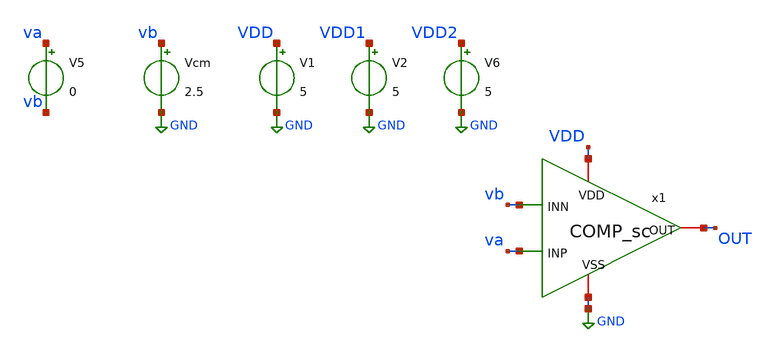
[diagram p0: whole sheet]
** sch_path: FINAL/XSCHEM/TEST_TOTAL/test_TOTAL.sch
**.subckt test_TOTAL
V1 VDD GND 5
V2 VDD1 GND 5
V6 VDD2 GND 5
V5 va vb 0
Vcm vb GND 2.5
x1 VDD vb OUT va GND COMP_sc
**** begin user architecture code

.include $::180MCU_MODELS/design.ngspice
.lib $::180MCU_MODELS/sm141064.ngspice typical
.lib $::180MCU_MODELS/sm141064.ngspice cap_mim
.lib $::180MCU_MODELS/sm141064.ngspice res_typical
.lib $::180MCU_MODELS/sm141064.ngspice moscap_typical
.lib $::180MCU_MODELS/sm141064.ngspice mimcap_typical


.include ../../../../Layouts/COMP/mag/COMP_pex_rc.spice
Xextrc GND VDD1 OUT1 va vb COMP
*COMP VSS VDD OUT INP INN


* The v2 layout, beside v1. The subcircuit is renamed to COMP_V2 because both
* extractions declare the same name -- the cell is named the same on purpose,
* which is what allows comparing them against the SAME reference in
* LVS. preparar_extraidos.sh renames it, touching only .subckt and .ends.
.include ../../../../layouts_v2/COMP/mag/COMP_V2_pex_rc.spice
Xextrc2 GND VDD2 OUT2 va vb COMP_V2



* CAREFUL: not one brace in this text. xschem counts them to find where the
* attribute block ends and a single one inside a comment cuts it in half,
* leaving the netlist with the template 'blabla' and raising no error.
*
* The inputs are gates, so the va/vb pair has no DC path to ground on its own.
* Vcm provides it. 2.5 V was chosen after sweeping it: unlike
* the OPAM, the COMP gain does not depend on common mode -- about
* 22000 V/V between 1.5 and 3.5 V -- because its output stage is properly
* dimensionada y no se sale de saturacion.
.save all
.control
* Wide window, to see the full swing of both branches.
dc V5 -0.3 0.3 1m
wrdata ancho.txt v(OUT) v(OUT1) v(OUT2) v(VDD)*i(v1) v(VDD1)*i(v2) v(VDD2)*i(v6)
plot v(OUT) v(OUT1) v(OUT2) title 'ANCHO'
plot v(VDD)*i(v1) v(VDD1)*i(v2) v(VDD2)*i(v6) title 'ANCHO'
* Fine window: at gain 22000 the transition is 5V/22000 = 227 uV, which the
* ventana de arriba se salta entera.
dc V5 -0.5m 0.5m 1u
wrdata fino.txt v(OUT) v(OUT1) v(OUT2)
plot v(OUT) v(OUT1) v(OUT2) title 'FINO'
plot v(VDD)*i(v1) v(VDD1)*i(v2) v(VDD2)*i(v6) title 'FINO'
.endc


**** end user architecture code
**.ends
.GLOBAL GND
.end
